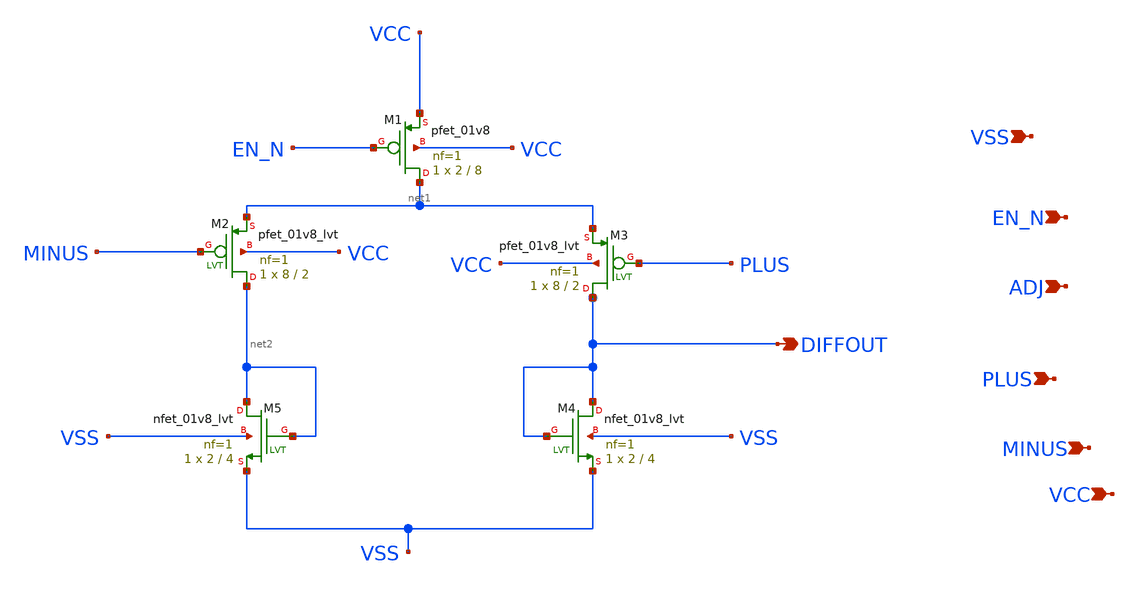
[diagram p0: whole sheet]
** sch_path: xschem/opamp.sch
**.subckt opamp PLUS MINUS VCC VSS EN_N ADJ DIFFOUT
*.ipin PLUS
*.ipin MINUS
*.ipin VCC
*.ipin VSS
*.ipin EN_N
*.ipin ADJ
*.opin DIFFOUT
XM1 net1 EN_N VCC VCC sky130_fd_pr__pfet_01v8 L=8 W=2 nf=1 ad='int((nf+1)/2) * W/nf * 0.29' as='int((nf+2)/2) * W/nf * 0.29'
+ pd='2*int((nf+1)/2) * (W/nf + 0.29)' ps='2*int((nf+2)/2) * (W/nf + 0.29)' nrd='0.29 / W' nrs='0.29 / W'
+ sa=0 sb=0 sd=0 mult=1 m=1
XM2 net2 MINUS net1 VCC sky130_fd_pr__pfet_01v8_lvt L=2 W=8 nf=1 ad='int((nf+1)/2) * W/nf * 0.29' as='int((nf+2)/2) * W/nf * 0.29'
+ pd='2*int((nf+1)/2) * (W/nf + 0.29)' ps='2*int((nf+2)/2) * (W/nf + 0.29)' nrd='0.29 / W' nrs='0.29 / W'
+ sa=0 sb=0 sd=0 mult=1 m=1
XM3 DIFFOUT PLUS net1 VCC sky130_fd_pr__pfet_01v8_lvt L=2 W=8 nf=1 ad='int((nf+1)/2) * W/nf * 0.29' as='int((nf+2)/2) * W/nf * 0.29'
+ pd='2*int((nf+1)/2) * (W/nf + 0.29)' ps='2*int((nf+2)/2) * (W/nf + 0.29)' nrd='0.29 / W' nrs='0.29 / W'
+ sa=0 sb=0 sd=0 mult=1 m=1
XM4 DIFFOUT DIFFOUT VSS VSS sky130_fd_pr__nfet_01v8_lvt L=4 W=2 nf=1 ad='int((nf+1)/2) * W/nf * 0.29'
+ as='int((nf+2)/2) * W/nf * 0.29' pd='2*int((nf+1)/2) * (W/nf + 0.29)' ps='2*int((nf+2)/2) * (W/nf + 0.29)'
+ nrd='0.29 / W' nrs='0.29 / W' sa=0 sb=0 sd=0 mult=1 m=1
XM5 net2 net2 VSS VSS sky130_fd_pr__nfet_01v8_lvt L=4 W=2 nf=1 ad='int((nf+1)/2) * W/nf * 0.29' as='int((nf+2)/2) * W/nf * 0.29'
+ pd='2*int((nf+1)/2) * (W/nf + 0.29)' ps='2*int((nf+2)/2) * (W/nf + 0.29)' nrd='0.29 / W' nrs='0.29 / W'
+ sa=0 sb=0 sd=0 mult=1 m=1
**.ends
.end
